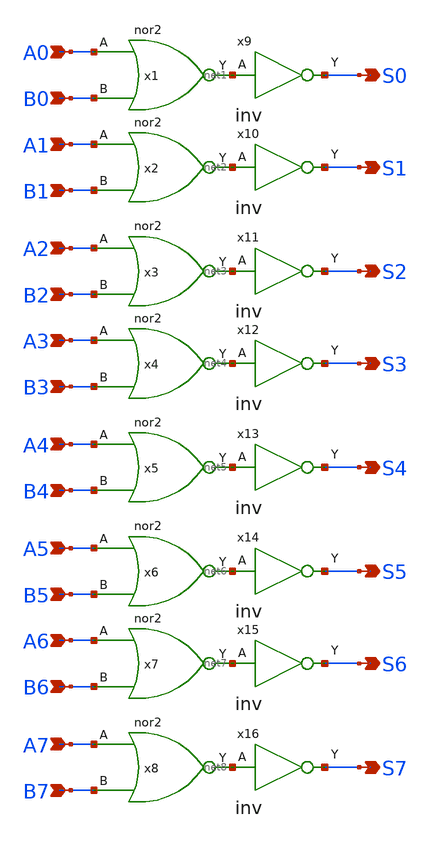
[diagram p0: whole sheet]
** sch_path: design/xschem/NOR/nor_8_bitwise.sch
**.subckt nor_8_bitwise S0 S1 S2 S3 S4 S5 S6 S7 A0 B0 A1 B1 A2 B2 A3 B3 A4 B4 A5 B5 A6 B6 A7 B7
*.opin S0
*.opin S1
*.opin S2
*.opin S3
*.opin S4
*.opin S5
*.opin S6
*.opin S7
*.ipin A0
*.ipin B0
*.ipin A1
*.ipin B1
*.ipin A2
*.ipin B2
*.ipin A3
*.ipin B3
*.ipin A4
*.ipin B4
*.ipin A5
*.ipin B5
*.ipin A6
*.ipin B6
*.ipin A7
*.ipin B7
x1 A0 B0 VSS VDD net1 nor2
x2 A1 B1 VSS VDD net2 nor2
x3 A2 B2 VSS VDD net3 nor2
x4 A3 B3 VSS VDD net4 nor2
x5 A4 B4 VSS VDD net5 nor2
x6 A5 B5 VSS VDD net6 nor2
x7 A6 B6 VSS VDD net7 nor2
x8 A7 B7 VSS VDD net8 nor2
x9 net1 VSS VDD S0 inv
x10 net2 VSS VDD S1 inv
x11 net3 VSS VDD S2 inv
x12 net4 VSS VDD S3 inv
x13 net5 VSS VDD S4 inv
x14 net6 VSS VDD S5 inv
x15 net7 VSS VDD S6 inv
x16 net8 VSS VDD S7 inv
**.ends
.end
